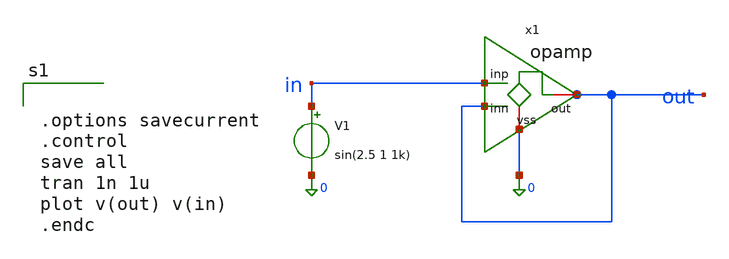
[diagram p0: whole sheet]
** sch_path: schema/untitled-1.sch
**.subckt untitled-1
x1 out in out 0 opamp
V1 in 0 sin(2.5 1 1k)
**** begin user architecture code


.options savecurrent
.control
save all
tran 1n 1u
plot v(out) v(in)
.endc


**** end user architecture code
**.ends

* expanding   symbol:  opamp.sym # of pins=4
** sym_path: schema/opamp.sym
** sch_path: schema/opamp.sch
.subckt opamp out inp inn vss
*.ipin inp
*.ipin inn
*.iopin out
*.iopin vss
E1 out vss inp inn 1e6
.ends

.end
